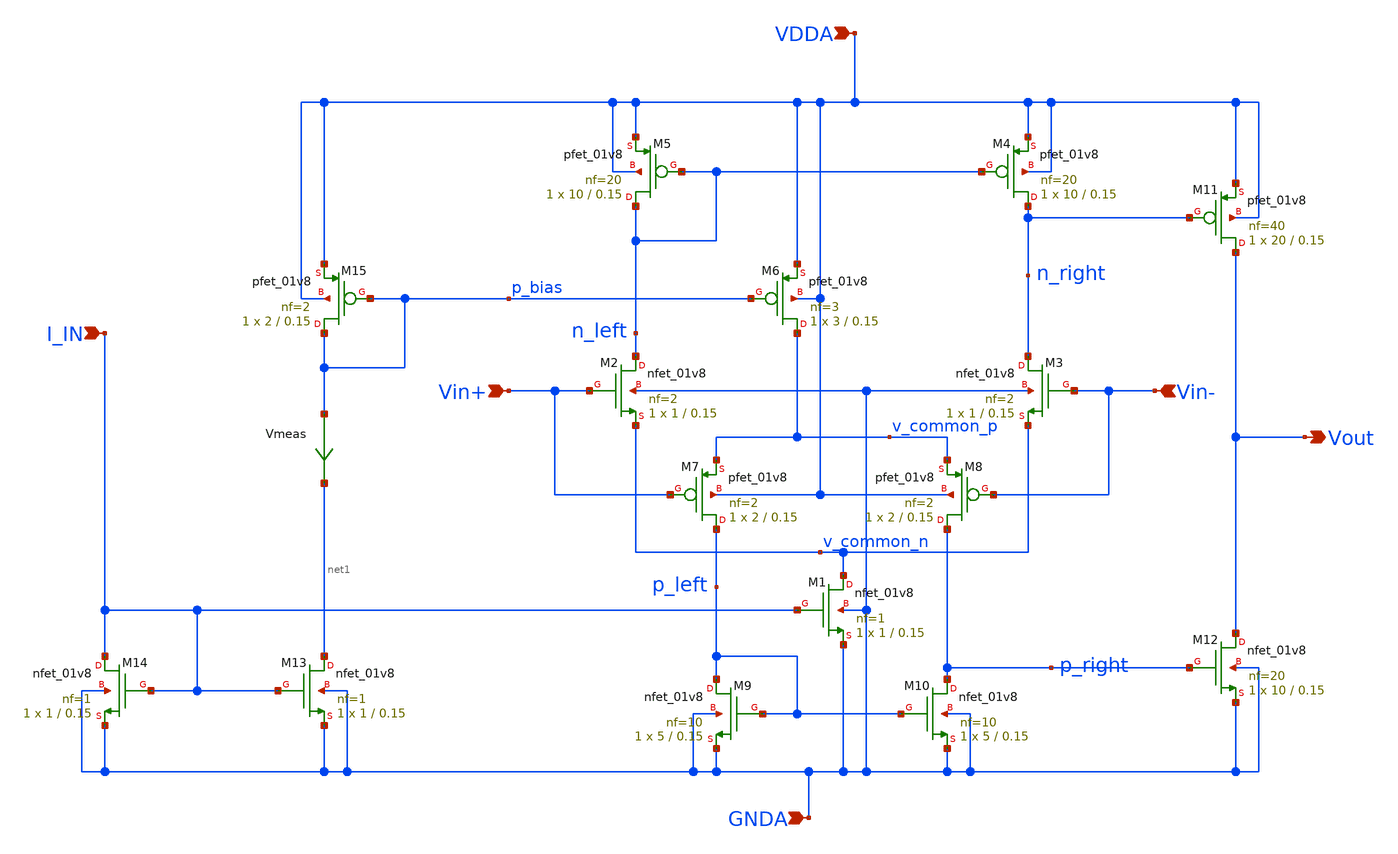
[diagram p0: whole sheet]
** sch_path: projects/pll/charge_pump/xschem_ngspice/rail_to_rail_opamp4.sch
**.subckt rail_to_rail_opamp4 Vout Vin+ Vin- VDDA GNDA I_IN
*.opin Vout
*.ipin Vin+
*.ipin Vin-
*.ipin VDDA
*.ipin GNDA
*.ipin I_IN
XM2 n_left Vin+ v_common_n GNDA sky130_fd_pr__nfet_01v8 L=0.15 W=1 nf=2 ad='int((nf+1)/2) * W/nf * 0.29'
+ as='int((nf+2)/2) * W/nf * 0.29' pd='2*int((nf+1)/2) * (W/nf + 0.29)' ps='2*int((nf+2)/2) * (W/nf + 0.29)'
+ nrd='0.29 / W' nrs='0.29 / W' sa=0 sb=0 sd=0 mult=1 m=1
XM3 n_right Vin- v_common_n GNDA sky130_fd_pr__nfet_01v8 L=0.15 W=1 nf=2 ad='int((nf+1)/2) * W/nf * 0.29'
+ as='int((nf+2)/2) * W/nf * 0.29' pd='2*int((nf+1)/2) * (W/nf + 0.29)' ps='2*int((nf+2)/2) * (W/nf + 0.29)'
+ nrd='0.29 / W' nrs='0.29 / W' sa=0 sb=0 sd=0 mult=1 m=1
XM5 n_left n_left VDDA VDDA sky130_fd_pr__pfet_01v8 L=0.15 W=10 nf=20 ad='int((nf+1)/2) * W/nf * 0.29'
+ as='int((nf+2)/2) * W/nf * 0.29' pd='2*int((nf+1)/2) * (W/nf + 0.29)' ps='2*int((nf+2)/2) * (W/nf + 0.29)'
+ nrd='0.29 / W' nrs='0.29 / W' sa=0 sb=0 sd=0 mult=1 m=1
XM4 n_right n_left VDDA VDDA sky130_fd_pr__pfet_01v8 L=0.15 W=10 nf=20 ad='int((nf+1)/2) * W/nf * 0.29'
+ as='int((nf+2)/2) * W/nf * 0.29' pd='2*int((nf+1)/2) * (W/nf + 0.29)' ps='2*int((nf+2)/2) * (W/nf + 0.29)'
+ nrd='0.29 / W' nrs='0.29 / W' sa=0 sb=0 sd=0 mult=1 m=1
XM6 v_common_p p_bias VDDA VDDA sky130_fd_pr__pfet_01v8 L=0.15 W=3 nf=3 ad='int((nf+1)/2) * W/nf * 0.29'
+ as='int((nf+2)/2) * W/nf * 0.29' pd='2*int((nf+1)/2) * (W/nf + 0.29)' ps='2*int((nf+2)/2) * (W/nf + 0.29)'
+ nrd='0.29 / W' nrs='0.29 / W' sa=0 sb=0 sd=0 mult=1 m=1
XM7 p_left Vin+ v_common_p VDDA sky130_fd_pr__pfet_01v8 L=0.15 W=2 nf=2 ad='int((nf+1)/2) * W/nf * 0.29'
+ as='int((nf+2)/2) * W/nf * 0.29' pd='2*int((nf+1)/2) * (W/nf + 0.29)' ps='2*int((nf+2)/2) * (W/nf + 0.29)'
+ nrd='0.29 / W' nrs='0.29 / W' sa=0 sb=0 sd=0 mult=1 m=1
XM8 p_right Vin- v_common_p VDDA sky130_fd_pr__pfet_01v8 L=0.15 W=2 nf=2 ad='int((nf+1)/2) * W/nf * 0.29'
+ as='int((nf+2)/2) * W/nf * 0.29' pd='2*int((nf+1)/2) * (W/nf + 0.29)' ps='2*int((nf+2)/2) * (W/nf + 0.29)'
+ nrd='0.29 / W' nrs='0.29 / W' sa=0 sb=0 sd=0 mult=1 m=1
XM9 p_left p_left GNDA GNDA sky130_fd_pr__nfet_01v8 L=0.15 W=5 nf=10 ad='int((nf+1)/2) * W/nf * 0.29'
+ as='int((nf+2)/2) * W/nf * 0.29' pd='2*int((nf+1)/2) * (W/nf + 0.29)' ps='2*int((nf+2)/2) * (W/nf + 0.29)'
+ nrd='0.29 / W' nrs='0.29 / W' sa=0 sb=0 sd=0 mult=1 m=1
XM10 p_right p_left GNDA GNDA sky130_fd_pr__nfet_01v8 L=0.15 W=5 nf=10 ad='int((nf+1)/2) * W/nf * 0.29'
+ as='int((nf+2)/2) * W/nf * 0.29' pd='2*int((nf+1)/2) * (W/nf + 0.29)' ps='2*int((nf+2)/2) * (W/nf + 0.29)'
+ nrd='0.29 / W' nrs='0.29 / W' sa=0 sb=0 sd=0 mult=1 m=1
XM1 v_common_n I_IN GNDA GNDA sky130_fd_pr__nfet_01v8 L=0.15 W=1 nf=1 ad='int((nf+1)/2) * W/nf * 0.29'
+ as='int((nf+2)/2) * W/nf * 0.29' pd='2*int((nf+1)/2) * (W/nf + 0.29)' ps='2*int((nf+2)/2) * (W/nf + 0.29)'
+ nrd='0.29 / W' nrs='0.29 / W' sa=0 sb=0 sd=0 mult=1 m=1
XM11 Vout n_right VDDA VDDA sky130_fd_pr__pfet_01v8 L=0.15 W=20 nf=40 ad='int((nf+1)/2) * W/nf * 0.29'
+ as='int((nf+2)/2) * W/nf * 0.29' pd='2*int((nf+1)/2) * (W/nf + 0.29)' ps='2*int((nf+2)/2) * (W/nf + 0.29)'
+ nrd='0.29 / W' nrs='0.29 / W' sa=0 sb=0 sd=0 mult=1 m=1
XM12 Vout p_right GNDA GNDA sky130_fd_pr__nfet_01v8 L=0.15 W=10 nf=20 ad='int((nf+1)/2) * W/nf * 0.29'
+ as='int((nf+2)/2) * W/nf * 0.29' pd='2*int((nf+1)/2) * (W/nf + 0.29)' ps='2*int((nf+2)/2) * (W/nf + 0.29)'
+ nrd='0.29 / W' nrs='0.29 / W' sa=0 sb=0 sd=0 mult=1 m=1
XM13 net1 I_IN GNDA GNDA sky130_fd_pr__nfet_01v8 L=0.15 W=1 nf=1 ad='int((nf+1)/2) * W/nf * 0.29' as='int((nf+2)/2) * W/nf * 0.29'
+ pd='2*int((nf+1)/2) * (W/nf + 0.29)' ps='2*int((nf+2)/2) * (W/nf + 0.29)' nrd='0.29 / W' nrs='0.29 / W'
+ sa=0 sb=0 sd=0 mult=1 m=1
XM15 p_bias p_bias VDDA VDDA sky130_fd_pr__pfet_01v8 L=0.15 W=2 nf=2 ad='int((nf+1)/2) * W/nf * 0.29'
+ as='int((nf+2)/2) * W/nf * 0.29' pd='2*int((nf+1)/2) * (W/nf + 0.29)' ps='2*int((nf+2)/2) * (W/nf + 0.29)'
+ nrd='0.29 / W' nrs='0.29 / W' sa=0 sb=0 sd=0 mult=1 m=1
Vmeas p_bias net1 0
.save i(vmeas)
XM14 I_IN I_IN GNDA GNDA sky130_fd_pr__nfet_01v8 L=0.15 W=1 nf=1 ad='int((nf+1)/2) * W/nf * 0.29' as='int((nf+2)/2) * W/nf * 0.29'
+ pd='2*int((nf+1)/2) * (W/nf + 0.29)' ps='2*int((nf+2)/2) * (W/nf + 0.29)' nrd='0.29 / W' nrs='0.29 / W'
+ sa=0 sb=0 sd=0 mult=1 m=1
**.ends
.end
